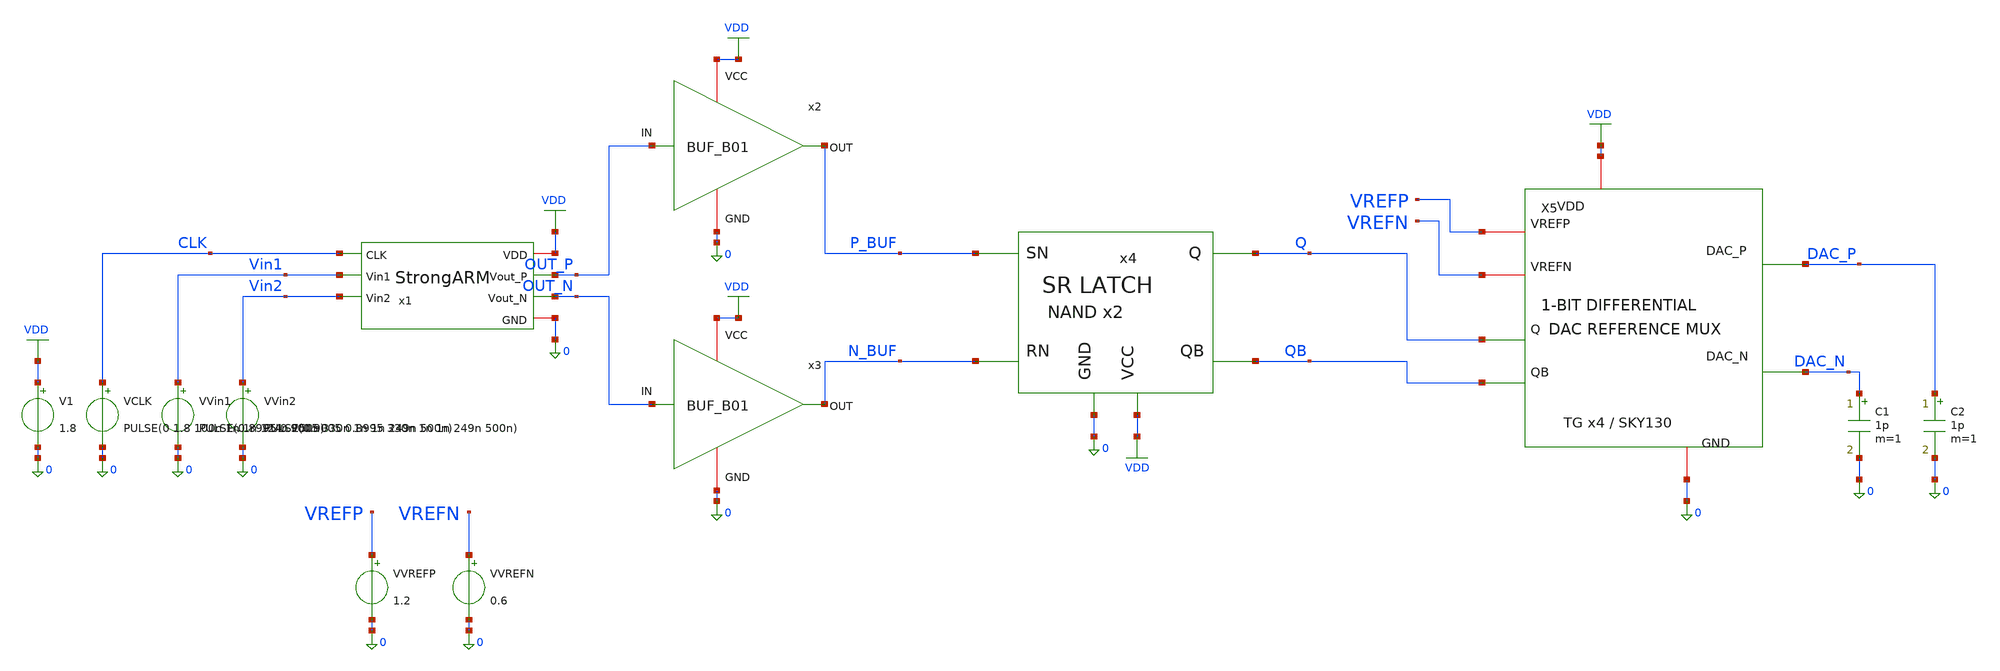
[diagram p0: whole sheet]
** sch_path: blocks/04_1Bit_DAC/sim/tb_4E_integration.sch
**.subckt tb_4E_integration
x1 VDD CLK OUT_P OUT_N Vin1 Vin2 0 StrongARM
x2 VDD OUT_P P_BUF 0 BUF_B01
x3 VDD OUT_N N_BUF 0 BUF_B01
x4 P_BUF N_BUF Q QB 0 VDD SR_Latch
X5 VREFP VREFN Q QB VDD 0 DAC_P DAC_N DAC_1bit
V1 VDD 0 1.8
VVin1 Vin1 0 PULSE(0.8995 0.9005 330n 1n 1n 249n 500n)
VVin2 Vin2 0 PULSE(0.9005 0.8995 330n 1n 1n 249n 500n)
VCLK CLK 0 PULSE(0 1.8 100n 1n 1n 124n 250n)
VVREFP VREFP 0 1.2
VVREFN VREFN 0 0.6
C1 DAC_N 0 1p m=1
C2 DAC_P 0 1p m=1
**** begin user architecture code


.lib /foss/pdks/sky130A/libs.tech/combined/sky130.lib.spice tt
.option scale=1e-6
.option reltol=1e-5 vntol=1e-8 abstol=1e-13
.temp 27

.tran 0.05n 3.1u 0 0.05n

.save v(Vin1) v(Vin2) v(CLK)
.save v(OUT_P) v(OUT_N) v(P_BUF) v(N_BUF)
.save v(Q) v(QB) v(DAC_P) v(DAC_N)

* Negative differential input: Vin1 < Vin2, expected Q=0, QB=1.8
.meas tran q_neg_200 FIND v(Q) AT=200n
.meas tran qb_neg_200 FIND v(QB) AT=200n
.meas tran dacp_neg_200 FIND v(DAC_P) AT=200n
.meas tran dacn_neg_200 FIND v(DAC_N) AT=200n

* Positive differential input: Vin1 > Vin2, expected Q=1.8, QB=0
.meas tran q_pos_450 FIND v(Q) AT=450n
.meas tran qb_pos_450 FIND v(QB) AT=450n
.meas tran dacp_pos_450 FIND v(DAC_P) AT=450n
.meas tran dacn_pos_450 FIND v(DAC_N) AT=450n

* Hold during comparator reset; these are spot checks, not full timing verification
.meas tran q_hold_neg_300 FIND v(Q) AT=300n
.meas tran q_hold_pos_550 FIND v(Q) AT=550n


**** end user architecture code
**.ends
.GLOBAL VDD
.end
